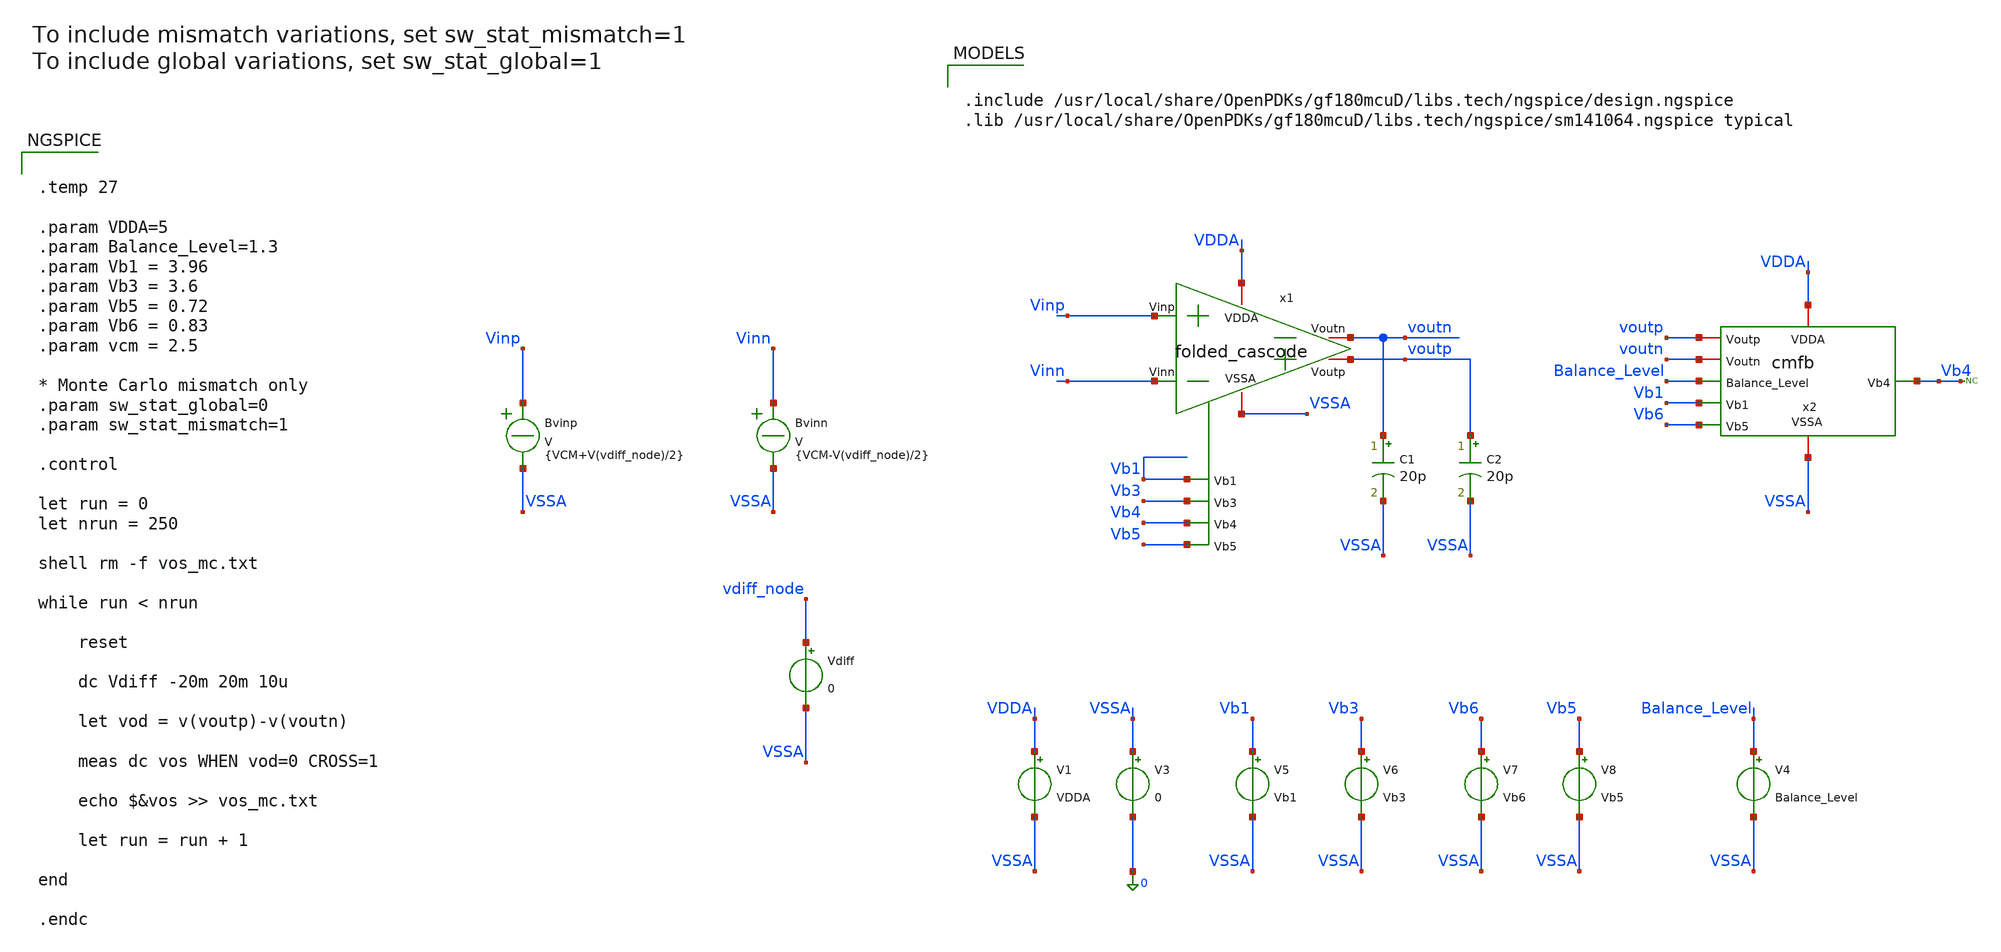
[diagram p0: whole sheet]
** sch_path: Folded_cascode/testbenches/simulation/fc_cmfb_offset_tb_batch.sch
**.subckt fc_cmfb_offset_tb_batch
x1 VDDA VSSA Vinp Vinn voutp voutn Vb1 Vb3 Vb4 Vb5 folded_cascode
x2 VDDA VSSA voutp voutn Balance_Level Vb1 Vb4 Vb6 cmfb
Vdiff vdiff_node VSSA 0
C1 voutn VSSA 20p m=1
C2 voutp VSSA 20p m=1
V1 VDDA VSSA VDDA
V3 VSSA 0 0
V5 Vb1 VSSA Vb1
V6 Vb3 VSSA Vb3
V4 Balance_Level VSSA Balance_Level
* noconn Vb4
Bvinp Vinp VSSA V = {VCM+V(vdiff_node)/2}
Bvinn Vinn VSSA V = {VCM-V(vdiff_node)/2}
V8 Vb5 VSSA Vb5
V7 Vb6 VSSA Vb6
**** begin user architecture code

.include /usr/local/share/OpenPDKs/gf180mcuD/libs.tech/ngspice/design.ngspice
.lib /usr/local/share/OpenPDKs/gf180mcuD/libs.tech/ngspice/sm141064.ngspice typical



.temp 27

.param VDDA=5
.param Balance_Level=1.3
.param Vb1 = 3.96
.param Vb3 = 3.6
.param Vb5 = 0.72
.param Vb6 = 0.83
.param vcm = 2.5

* Monte Carlo mismatch only
.param sw_stat_global=0
.param sw_stat_mismatch=1

.control

let run = 0
let nrun = 250

shell rm -f vos_mc.txt

while run < nrun

    reset

    dc Vdiff -20m 20m 10u

    let vod = v(voutp)-v(voutn)

    meas dc vos WHEN vod=0 CROSS=1

    echo $&vos >> vos_mc.txt

    let run = run + 1

end

.endc


**** end user architecture code
**.ends
.end
